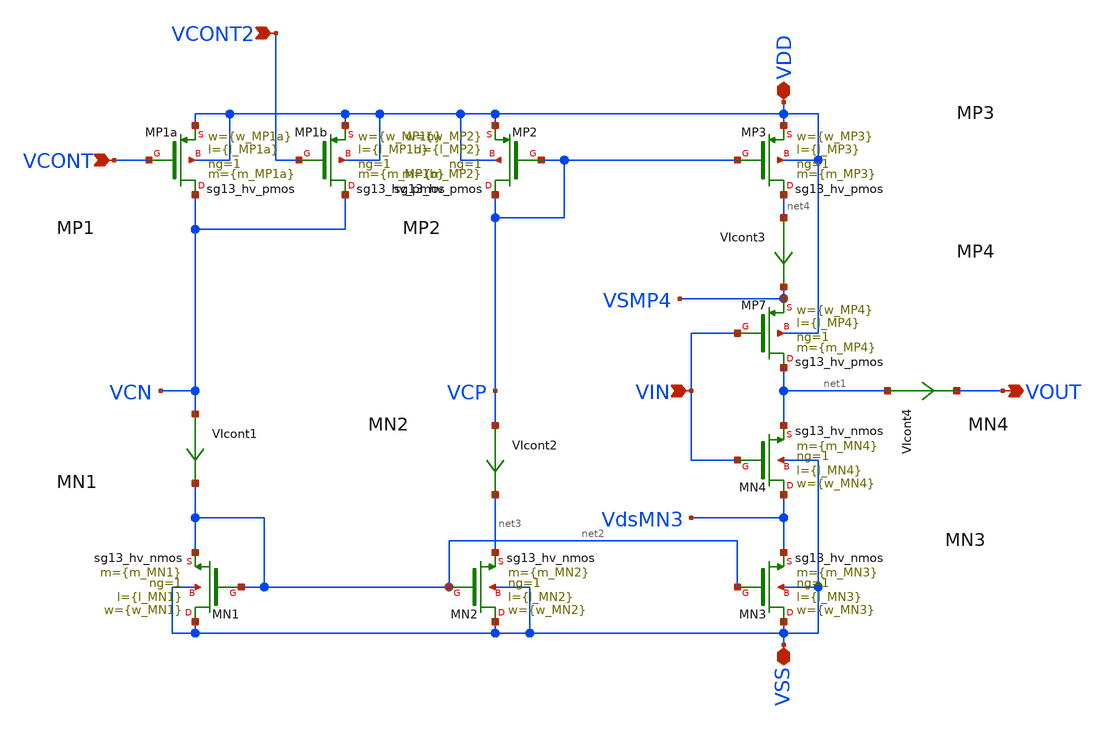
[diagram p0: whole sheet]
** sch_path: xschem/VCO/stage_V1.sch
**.subckt stage_V1 VCONT2 VIN VOUT VDD VSS VCONT
*.ipin VCONT2
*.ipin VIN
*.opin VOUT
*.iopin VDD
*.iopin VSS
*.ipin VCONT
XMN1 VSS net2 net2 VSS sg13_hv_nmos w={w_MN1} l={l_MN1} ng=1 m={m_MN1} mm_ok=1
XMN2 VSS net2 net3 VSS sg13_hv_nmos w={w_MN2} l={l_MN2} ng=1 m={m_MN2} mm_ok=1
XMN3 VSS net2 VdsMN3 VSS sg13_hv_nmos w={w_MN3} l={l_MN3} ng=1 m={m_MN3} mm_ok=1
XMP1a VCN VCONT VDD VDD sg13_hv_pmos w={w_MP1a} l={l_MP1a} ng=1 m={m_MP1a} mm_ok=1
XMP2 VCP VCP VDD VDD sg13_hv_pmos w={w_MP2} l={l_MP2} ng=1 m={m_MP2} mm_ok=1
XMP3 net4 VCP VDD VDD sg13_hv_pmos w={w_MP3} l={l_MP3} ng=1 m={m_MP3} mm_ok=1
XMP7 net1 VIN VSMP4 VDD sg13_hv_pmos w={w_MP4} l={l_MP4} ng=1 m={m_MP4} mm_ok=1
XMN4 VdsMN3 VIN net1 VSS sg13_hv_nmos w={w_MN4} l={l_MN4} ng=1 m={m_MN4} mm_ok=1
XMP1b VCN VCONT2 VDD VDD sg13_hv_pmos w={w_MP1b} l={l_MP1b} ng=1 m={m_MP1b} mm_ok=1
VIcont1 VCN net2 0
.save i(vicont1)
VIcont2 VCP net3 0
.save i(vicont2)
VIcont3 net4 VSMP4 0
.save i(vicont3)
VIcont4 net1 VOUT 0
.save i(vicont4)
**.ends
.end
